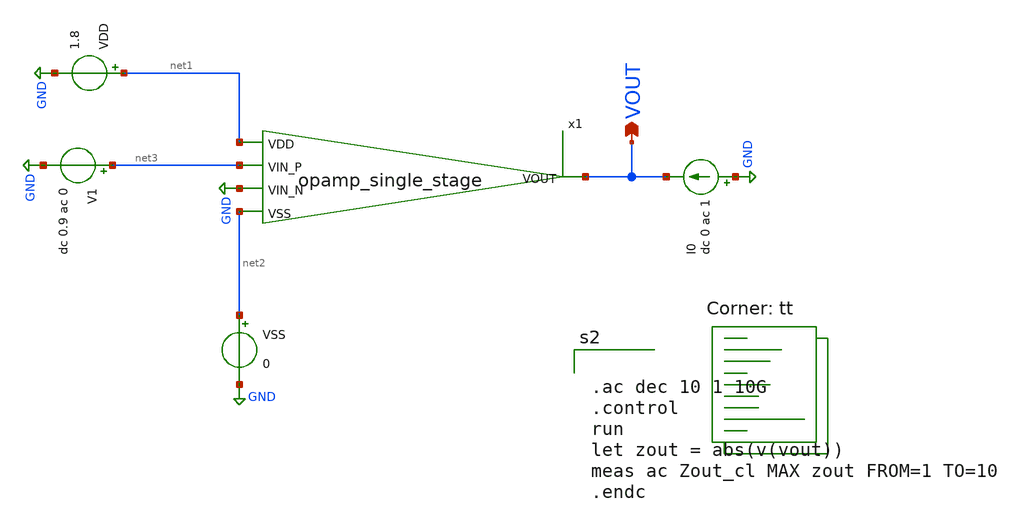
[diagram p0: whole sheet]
** sch_path: analog/schematics/testbenches/tb_out_impedence.sch
**.subckt tb_out_impedence VOUT
*.opin VOUT
x1 net1 VOUT net3 GND net2 opamp_single_stage
VDD net1 GND 1.8
VSS net2 GND 0
V1 net3 GND dc 0.9 ac 0
I0 GND VOUT dc 0 ac 1
**** begin user architecture code
.lib $::SKYWATER_MODELS/sky130.lib.spice tt


.ac dec 10 1 10G
.control
run
let zout = abs(v(vout))
meas ac Zout_cl MAX zout FROM=1 TO=10
.endc




**** end user architecture code
**.ends

* expanding   symbol:  opamp_single_stage.sym # of pins=5
** sym_path: analog/schematics/opamp_single_stage.sym
** sch_path: analog/schematics/opamp_single_stage.sch
.subckt opamp_single_stage VDD VOUT VIN_P VIN_N VSS
*.ipin VDD
*.ipin VIN_P
*.ipin VSS
*.opin VOUT
*.ipin VIN_N
XM4 net2 net1 VDD VDD sky130_fd_pr__pfet_01v8 L=0.5 W=8 nf=1 ad='int((nf+1)/2) * W/nf * 0.29' as='int((nf+2)/2) * W/nf * 0.29'
+ pd='2*int((nf+1)/2) * (W/nf + 0.29)' ps='2*int((nf+2)/2) * (W/nf + 0.29)' nrd='0.29 / W' nrs='0.29 / W'
+ sa=0 sb=0 sd=0 mult=1 m=1
XM3 net1 net1 VDD VDD sky130_fd_pr__pfet_01v8 L=0.5 W=8 nf=1 ad='int((nf+1)/2) * W/nf * 0.29' as='int((nf+2)/2) * W/nf * 0.29'
+ pd='2*int((nf+1)/2) * (W/nf + 0.29)' ps='2*int((nf+2)/2) * (W/nf + 0.29)' nrd='0.29 / W' nrs='0.29 / W'
+ sa=0 sb=0 sd=0 mult=1 m=1
XM1 net1 VIN_N net3 GND sky130_fd_pr__nfet_01v8_lvt L=0.5 W=6 nf=1 ad='int((nf+1)/2) * W/nf * 0.29' as='int((nf+2)/2) * W/nf * 0.29'
+ pd='2*int((nf+1)/2) * (W/nf + 0.29)' ps='2*int((nf+2)/2) * (W/nf + 0.29)' nrd='0.29 / W' nrs='0.29 / W'
+ sa=0 sb=0 sd=0 mult=1 m=1
XM2 net2 VIN_P net3 GND sky130_fd_pr__nfet_01v8_lvt L=0.5 W=6 nf=1 ad='int((nf+1)/2) * W/nf * 0.29' as='int((nf+2)/2) * W/nf * 0.29'
+ pd='2*int((nf+1)/2) * (W/nf + 0.29)' ps='2*int((nf+2)/2) * (W/nf + 0.29)' nrd='0.29 / W' nrs='0.29 / W'
+ sa=0 sb=0 sd=0 mult=1 m=1
XM5 VOUT net2 VDD VDD sky130_fd_pr__pfet_01v8 L=0.5 W=20 nf=1 ad='int((nf+1)/2) * W/nf * 0.29' as='int((nf+2)/2) * W/nf * 0.29'
+ pd='2*int((nf+1)/2) * (W/nf + 0.29)' ps='2*int((nf+2)/2) * (W/nf + 0.29)' nrd='0.29 / W' nrs='0.29 / W'
+ sa=0 sb=0 sd=0 mult=1 m=1
XC1 net5 VOUT sky130_fd_pr__cap_mim_m3_1 W=25 L=20 MF=1 m=1
XM8 net4 net4 VSS VSS sky130_fd_pr__nfet_01v8_lvt L=1.0 W=2 nf=1 ad='int((nf+1)/2) * W/nf * 0.29' as='int((nf+2)/2) * W/nf * 0.29'
+ pd='2*int((nf+1)/2) * (W/nf + 0.29)' ps='2*int((nf+2)/2) * (W/nf + 0.29)' nrd='0.29 / W' nrs='0.29 / W'
+ sa=0 sb=0 sd=0 mult=1 m=1
XM7 net3 net4 VSS VSS sky130_fd_pr__nfet_01v8_lvt L=1.0 W=4 nf=1 ad='int((nf+1)/2) * W/nf * 0.29' as='int((nf+2)/2) * W/nf * 0.29'
+ pd='2*int((nf+1)/2) * (W/nf + 0.29)' ps='2*int((nf+2)/2) * (W/nf + 0.29)' nrd='0.29 / W' nrs='0.29 / W'
+ sa=0 sb=0 sd=0 mult=1 m=1
XM6 VOUT net4 VSS VSS sky130_fd_pr__nfet_01v8_lvt L=1.0 W=8 nf=1 ad='int((nf+1)/2) * W/nf * 0.29' as='int((nf+2)/2) * W/nf * 0.29'
+ pd='2*int((nf+1)/2) * (W/nf + 0.29)' ps='2*int((nf+2)/2) * (W/nf + 0.29)' nrd='0.29 / W' nrs='0.29 / W'
+ sa=0 sb=0 sd=0 mult=1 m=1
R1 net5 net2 7k m=1
XR2 net4 VDD VDD sky130_fd_pr__res_high_po W=0.35 L=14 mult=1 m=1
.ends

.GLOBAL GND
.end
